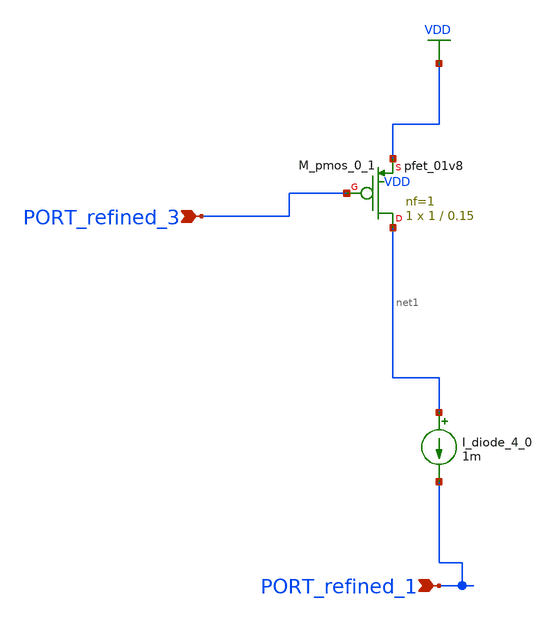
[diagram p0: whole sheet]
** sch_path: schematics/AMSNet/7.sch
**.subckt 7 PORT_refined_3 PORT_refined_1
*.ipin PORT_refined_3
*.ipin PORT_refined_1
I_diode_4_0 net1 PORT_refined_1 1m
XM_pmos_0_1 net1 PORT_refined_3 VDD VDD sky130_fd_pr__pfet_01v8 L=0.15 W=1 nf=1 ad='int((1 + 1)/2) * 1 / 1 * 0.29'
+ as='int((1 + 2)/2) * 1 / 1 * 0.29' pd='2*int((1 + 1)/2) * (1 / 1 + 0.29)' ps='2*int((1 + 2)/2) * (1 / 1 + 0.29)'
+ nrd='0.29 / 1 ' nrs='0.29 / 1 ' sa=0 sb=0 sd=0 mult=1 m=1
**.ends
.GLOBAL VDD
.end
